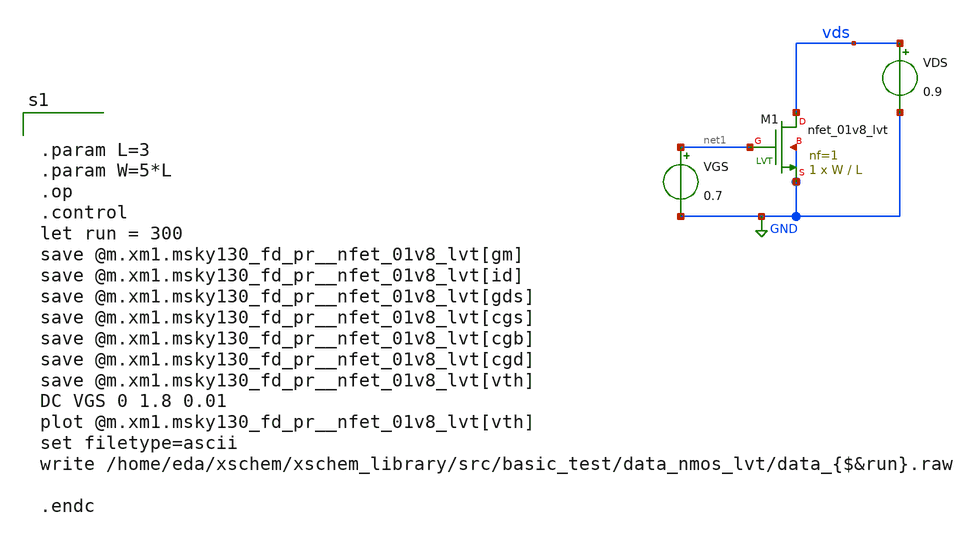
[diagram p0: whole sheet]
** sch_path: xschem/src/basic_test/gm_id_nmos.sch
**.subckt gm_id_nmos
VDS vds GND 0.9
XM1 vds net1 GND GND sky130_fd_pr__nfet_01v8_lvt L=L W=W nf=1 ad='int((nf+1)/2) * W/nf * 0.29' as='int((nf+2)/2) * W/nf * 0.29'
+ pd='2*int((nf+1)/2) * (W/nf + 0.29)' ps='2*int((nf+2)/2) * (W/nf + 0.29)' nrd='0.29 / W' nrs='0.29 / W'
+ sa=0 sb=0 sd=0 mult=1 m=1
VGS net1 GND 0.7
**** begin user architecture code


.param L=3
.param W=5*L
.op
.control
let run = 300
save @m.xm1.msky130_fd_pr__nfet_01v8_lvt[gm]
save @m.xm1.msky130_fd_pr__nfet_01v8_lvt[id]
save @m.xm1.msky130_fd_pr__nfet_01v8_lvt[gds]
save @m.xm1.msky130_fd_pr__nfet_01v8_lvt[cgs]
save @m.xm1.msky130_fd_pr__nfet_01v8_lvt[cgb]
save @m.xm1.msky130_fd_pr__nfet_01v8_lvt[cgd]
save @m.xm1.msky130_fd_pr__nfet_01v8_lvt[vth]
DC VGS 0 1.8 0.01
plot @m.xm1.msky130_fd_pr__nfet_01v8_lvt[vth]
set filetype=ascii
write /home/eda/xschem/xschem_library/src/basic_test/data_nmos_lvt/data_{$&run}.raw

.endc




.include $::SKYWATER_MODELS/cells/nfet_01v8/sky130_fd_pr__nfet_01v8__tt.corner.spice
.include $::SKYWATER_MODELS/cells/nfet_01v8_lvt/sky130_fd_pr__nfet_01v8_lvt__tt.corner.spice
.include $::SKYWATER_MODELS/cells/pfet_01v8/sky130_fd_pr__pfet_01v8__tt.corner.spice
.include $::SKYWATER_MODELS/cells/nfet_03v3_nvt/sky130_fd_pr__nfet_03v3_nvt__tt.corner.spice
.include $::SKYWATER_MODELS/cells/nfet_05v0_nvt/sky130_fd_pr__nfet_05v0_nvt__tt.corner.spice
.include $::SKYWATER_MODELS/cells/esd_nfet_01v8/sky130_fd_pr__esd_nfet_01v8__tt.corner.spice
.include $::SKYWATER_MODELS/cells/pfet_01v8_lvt/sky130_fd_pr__pfet_01v8_lvt__tt.corner.spice
.include $::SKYWATER_MODELS/cells/pfet_01v8_hvt/sky130_fd_pr__pfet_01v8_hvt__tt.corner.spice
.include $::SKYWATER_MODELS/cells/esd_pfet_g5v0d10v5/sky130_fd_pr__esd_pfet_g5v0d10v5__tt.corner.spice
.include $::SKYWATER_MODELS/cells/pfet_g5v0d10v5/sky130_fd_pr__pfet_g5v0d10v5__tt.corner.spice
.include $::SKYWATER_MODELS/cells/pfet_g5v0d16v0/sky130_fd_pr__pfet_g5v0d16v0__tt.corner.spice
.include $::SKYWATER_MODELS/cells/nfet_g5v0d10v5/sky130_fd_pr__nfet_g5v0d10v5__tt.corner.spice
.include $::SKYWATER_MODELS/cells/nfet_g5v0d16v0/sky130_fd_pr__nfet_g5v0d16v0__tt_discrete.corner.spice
.include $::SKYWATER_MODELS/cells/esd_nfet_g5v0d10v5/sky130_fd_pr__esd_nfet_g5v0d10v5__tt.corner.spice
.include $::SKYWATER_MODELS/models/corners/tt/nonfet.spice
* Mismatch parameters
.include $::SKYWATER_MODELS/cells/nfet_01v8/sky130_fd_pr__nfet_01v8__mismatch.corner.spice
.include $::SKYWATER_MODELS/cells/pfet_01v8/sky130_fd_pr__pfet_01v8__mismatch.corner.spice
.include $::SKYWATER_MODELS/cells/nfet_01v8_lvt/sky130_fd_pr__nfet_01v8_lvt__mismatch.corner.spice
.include $::SKYWATER_MODELS/cells/pfet_01v8_lvt/sky130_fd_pr__pfet_01v8_lvt__mismatch.corner.spice
.include $::SKYWATER_MODELS/cells/pfet_01v8_hvt/sky130_fd_pr__pfet_01v8_hvt__mismatch.corner.spice
.include $::SKYWATER_MODELS/cells/nfet_g5v0d10v5/sky130_fd_pr__nfet_g5v0d10v5__mismatch.corner.spice
.include $::SKYWATER_MODELS/cells/pfet_g5v0d10v5/sky130_fd_pr__pfet_g5v0d10v5__mismatch.corner.spice
.include $::SKYWATER_MODELS/cells/nfet_05v0_nvt/sky130_fd_pr__nfet_05v0_nvt__mismatch.corner.spice
.include $::SKYWATER_MODELS/cells/nfet_03v3_nvt/sky130_fd_pr__nfet_03v3_nvt__mismatch.corner.spice
* Resistor$::SKYWATER_MODELS/Capacitor
.include $::SKYWATER_MODELS/models/r+c/res_typical__cap_typical.spice
.include $::SKYWATER_MODELS/models/r+c/res_typical__cap_typical__lin.spice
* Special cells
.include $::SKYWATER_MODELS/models/corners/tt/specialized_cells.spice
* All models
.include $::SKYWATER_MODELS/models/all.spice
* Corner
.include $::SKYWATER_MODELS/models/corners/tt/rf.spice

**** end user architecture code
**.ends
.GLOBAL GND
.end
